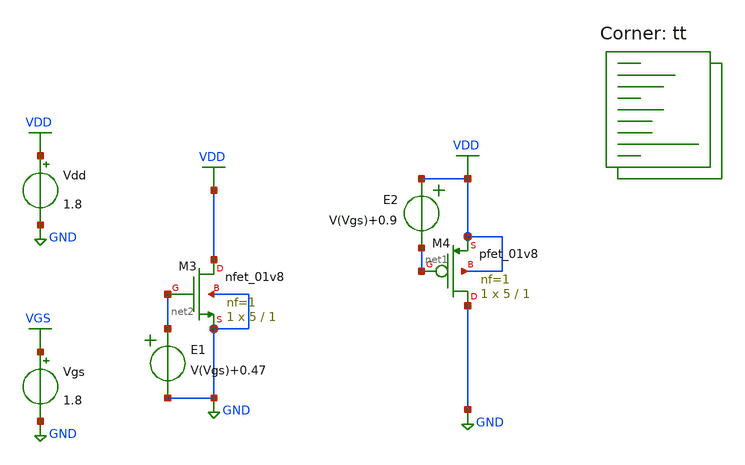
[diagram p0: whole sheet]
** sch_path: mobility.sch
**.subckt mobility
Vgs VGS GND 1.8
Vdd VDD GND 1.8
XM3 VDD net2 GND GND sky130_fd_pr__nfet_01v8 L=1 W=5 nf=1 ad='int((nf+1)/2) * W/nf * 0.29' as='int((nf+2)/2) * W/nf * 0.29'
+ pd='2*int((nf+1)/2) * (W/nf + 0.29)' ps='2*int((nf+2)/2) * (W/nf + 0.29)' nrd='0.29 / W' nrs='0.29 / W'
+ sa=0 sb=0 sd=0 mult=1 m=1
XM4 GND net1 VDD VDD sky130_fd_pr__pfet_01v8 L=1 W=5 nf=1 ad='int((nf+1)/2) * W/nf * 0.29' as='int((nf+2)/2) * W/nf * 0.29'
+ pd='2*int((nf+1)/2) * (W/nf + 0.29)' ps='2*int((nf+2)/2) * (W/nf + 0.29)' nrd='0.29 / W' nrs='0.29 / W'
+ sa=0 sb=0 sd=0 mult=1 m=1
E1 net2 GND VOL=' V(Vgs)+0.47 '
E2 VDD net1 VOL=' V(Vgs)+0.9 '
**** begin user architecture code



.options savecurrents

.control
save all
*dc vgs 0 1.8 0.01 vdd 0.01 1.8 0.2
*dc vdd 0.01 1.8 0.01
dc vgs 0 1.8 0.01
let id_nmos=@m.xm3.msky130_fd_pr__nfet_01v8[id]
let id_pmos=@m.xm4.msky130_fd_pr__pfet_01v8[id]

plot deriv(sqrt(id_nmos))^2/deriv(sqrt(id_pmos))^2 title 'V_DD characteristic' xlabel 'V_DD' ylabel 'Ratio of derivatives'

write characterization.raw

set appendwrite
.endc


.lib $::SKYWATER_MODELS/sky130.lib.spice tt
**** end user architecture code
**.ends
.GLOBAL GND
.GLOBAL VGS
.GLOBAL VDD
.end
